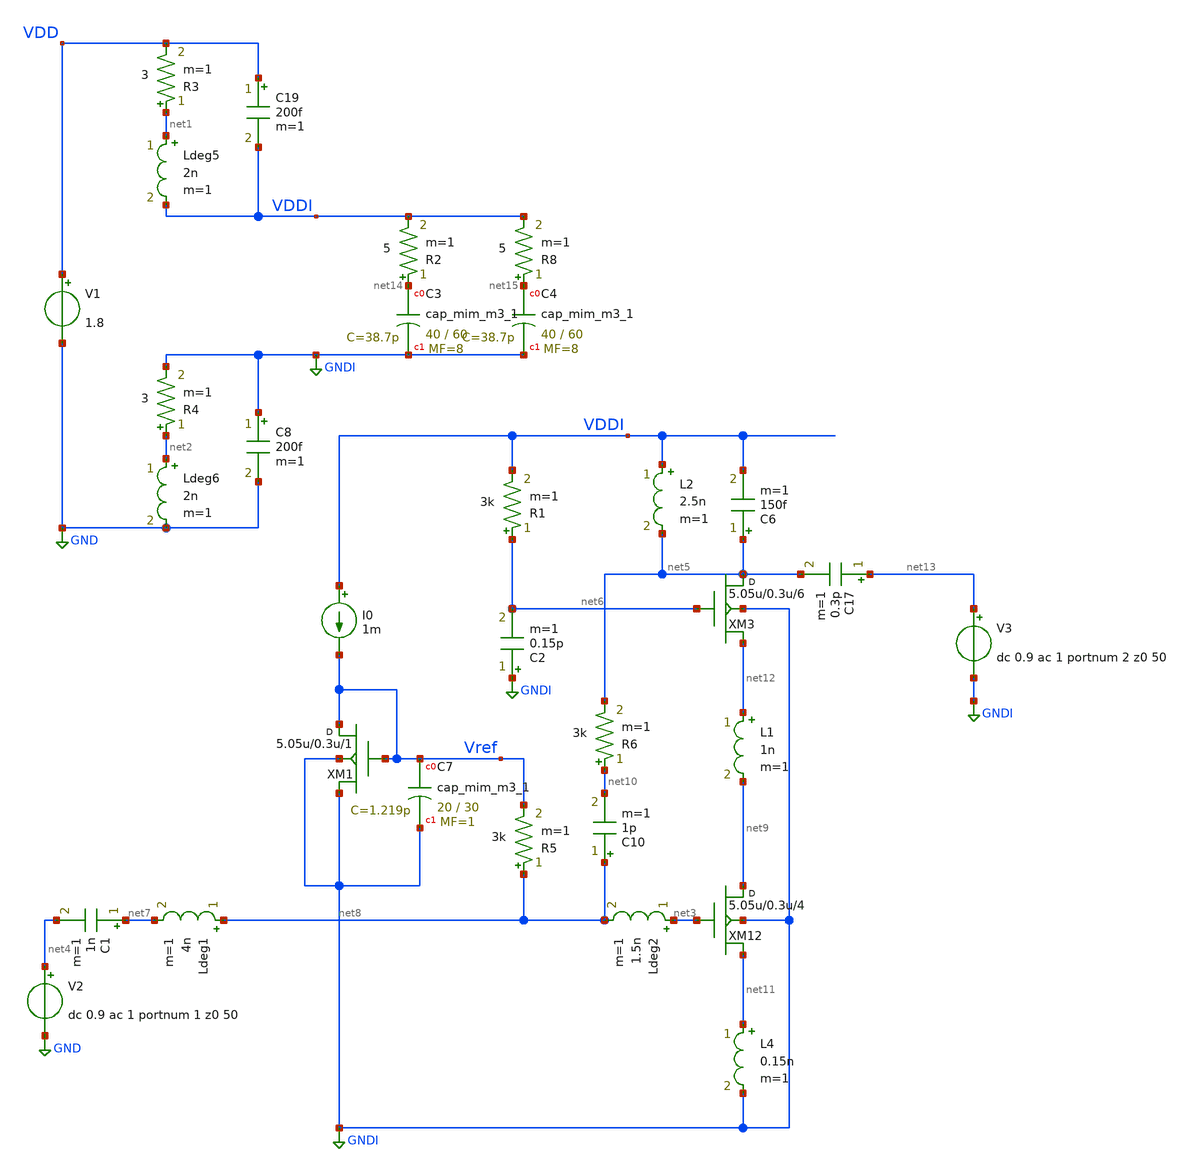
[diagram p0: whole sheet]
** sch_path: xschem/LNA5_with_output_buf_3_SP.sch
**.subckt LNA5_with_output_buf_3_SP
V1 VDD GND 1.8
V2 net4 GND dc 0.9 ac 1 portnum 1 z0 50
I0 VDDI Vref 1m
XM1 Vref Vref GNDI GNDI sky130_fd_pr__rf_nfet_01v8_bM04W5p00L0p15_ext w=5.05u l=0.3u m=1
XC7 Vref GNDI sky130_fd_pr__cap_mim_m3_1 W=20 L=30 MF=1 m=1
Ldeg5 net1 VDDI 2n m=1
R3 net1 VDD 3 m=1
Ldeg6 net2 GND 2n m=1
R4 net2 GNDI 3 m=1
XM12 net9 net3 net11 GNDI sky130_fd_pr__rf_nfet_01v8_bM04W5p00L0p15_ext w=5.05u l=0.3u m=4
C17 net13 net5 0.3p m=1
L2 VDDI net5 2.5n m=1
XC3 net14 GNDI sky130_fd_pr__cap_mim_m3_1 W=40 L=60 MF=8 m=8
C8 GNDI GND 200f m=1
C19 VDD VDDI 200f m=1
R2 net14 VDDI 5 m=1
R5 net8 Vref 3k m=1
C1 net7 net4 1n m=1
C6 net5 VDDI 150f m=1
R6 net10 net5 3k m=1
XM3 net5 net6 net12 GNDI sky130_fd_pr__rf_nfet_01v8_bM04W5p00L0p15_ext w=5.05u l=0.3u m=6
Ldeg1 net8 net7 4n m=1
L1 net12 net9 1n m=1
Ldeg2 net3 net8 1.5n m=1
XC4 net15 GNDI sky130_fd_pr__cap_mim_m3_1 W=40 L=60 MF=8 m=8
R8 net15 VDDI 5 m=1
C10 net8 net10 1p m=1
L4 net11 GNDI 0.15n m=1
V3 net13 GNDI dc 0.9 ac 1 portnum 2 z0 50
R1 net6 VDDI 3k m=1
C2 GNDI net6 0.15p m=1
**** begin user architecture code


.subckt sky130_fd_pr__rf_nfet_01v8_bM04W5p00L0p15_ext DRAIN GATE SOURCE SUBSTRATE
X0 DRAIN GATE SOURCE SUBSTRATE sky130_fd_pr__nfet_01v8 ad=2.828e+12p pd=2.132e+07u as=4.242e+12p
+ ps=3.198e+07u w=5.05e+06u l=150000u
X1 SOURCE SUBSTRATE SUBSTRATE SUBSTRATE sky130_fd_pr__nfet_01v8 ad=0p pd=0u as=3.03e+12p
+ ps=2.14e+07u w=5.05e+06u l=150000u
X2 SOURCE GATE DRAIN SUBSTRATE sky130_fd_pr__nfet_01v8 ad=0p pd=0u as=0p ps=0u w=5.05e+06u l=150000u
X3 DRAIN GATE SOURCE SUBSTRATE sky130_fd_pr__nfet_01v8 ad=0p pd=0u as=0p ps=0u w=5.05e+06u l=150000u
X4 SUBSTRATE SUBSTRATE SOURCE SUBSTRATE sky130_fd_pr__nfet_01v8 ad=0p pd=0u as=0p ps=0u w=5.05e+06u
+ l=150000u
X5 SOURCE GATE DRAIN SUBSTRATE sky130_fd_pr__nfet_01v8 ad=0p pd=0u as=0p ps=0u w=5.05e+06u l=150000u
.ends
.sp dec 1000 0.1e9 100e9 1
* .ac dec 1000 0.01e9 100e9
.control
run
display
let z11=50*(1+s_1_1)/(1-s_1_1)
let z22=50*(1+s_2_2)/(1-s_2_2)
let S11 = S_1_1
let S21 = S_2_1
let S12 = S_1_2
let S22 = S_2_2

* Stability
let delta=S11*S22-S12*S21
let K    = (1-mag(S11)^2-mag(S22)^2+mag(delta)^2)/(2*mag(S12*S21))
let mu   = (1-mag(S11)^2)/(mag(S22-conj(S11)*delta)+mag(S21*S12))
* plot real(z11) real(z22)
* plot imag(z11) imag(z22)
plot db(S_1_1) db(S_2_2) db(S_2_1)

plot db(K)
plot mag(delta)
plot db(mu)
plot NF NFmin
.endc


.lib $::SKYWATER_MODELS/sky130.lib.spice tt
* .include $::PDKPATH/libs.ref/sky130_fd_sc_hvl/spice/sky130_fd_sc_hvl.spice

**** end user architecture code
**.ends
.GLOBAL GND
.GLOBAL GNDI
.end
